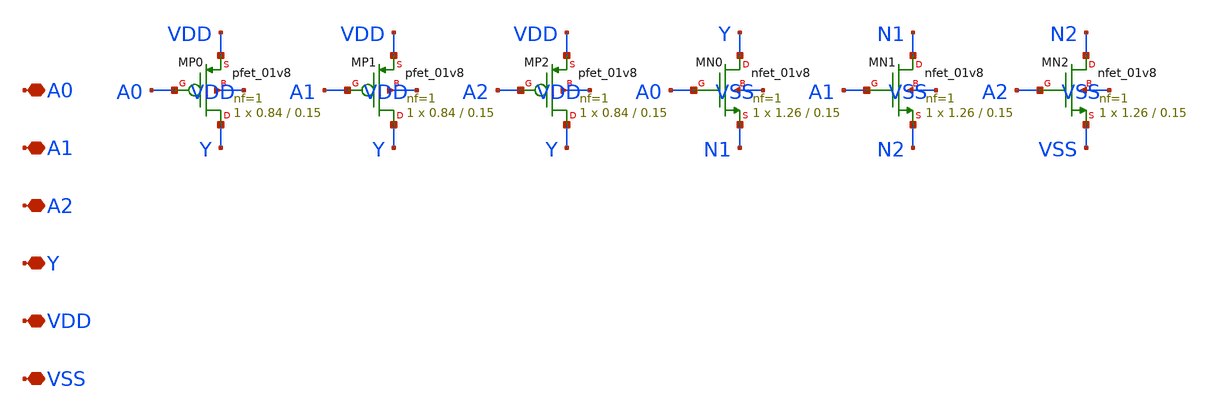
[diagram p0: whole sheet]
** sch_path: design/compiler/cells/sram_nand3.sch
**.subckt sram_nand3 A0 A1 A2 Y VDD VSS
*.iopin A0
*.iopin A1
*.iopin A2
*.iopin Y
*.iopin VDD
*.iopin VSS
XMP0 Y A0 VDD VDD sky130_fd_pr__pfet_01v8 L=0.15 W=0.84 nf=1 ad=0.2436 as=0.2436 pd=2.26 ps=2.26
+ nrd=0.3452 nrs=0.3452 sa=0 sb=0 sd=0 mult=1 m=1
XMP1 Y A1 VDD VDD sky130_fd_pr__pfet_01v8 L=0.15 W=0.84 nf=1 ad=0.2436 as=0.2436 pd=2.26 ps=2.26
+ nrd=0.3452 nrs=0.3452 sa=0 sb=0 sd=0 mult=1 m=1
XMP2 Y A2 VDD VDD sky130_fd_pr__pfet_01v8 L=0.15 W=0.84 nf=1 ad=0.2436 as=0.2436 pd=2.26 ps=2.26
+ nrd=0.3452 nrs=0.3452 sa=0 sb=0 sd=0 mult=1 m=1
XMN0 Y A0 N1 VSS sky130_fd_pr__nfet_01v8 L=0.15 W=1.26 nf=1 ad=0.3654 as=0.3654 pd=3.1 ps=3.1
+ nrd=0.2302 nrs=0.2302 sa=0 sb=0 sd=0 mult=1 m=1
XMN1 N1 A1 N2 VSS sky130_fd_pr__nfet_01v8 L=0.15 W=1.26 nf=1 ad=0.3654 as=0.3654 pd=3.1 ps=3.1
+ nrd=0.2302 nrs=0.2302 sa=0 sb=0 sd=0 mult=1 m=1
XMN2 N2 A2 VSS VSS sky130_fd_pr__nfet_01v8 L=0.15 W=1.26 nf=1 ad=0.3654 as=0.3654 pd=3.1 ps=3.1
+ nrd=0.2302 nrs=0.2302 sa=0 sb=0 sd=0 mult=1 m=1
**.ends
.end
